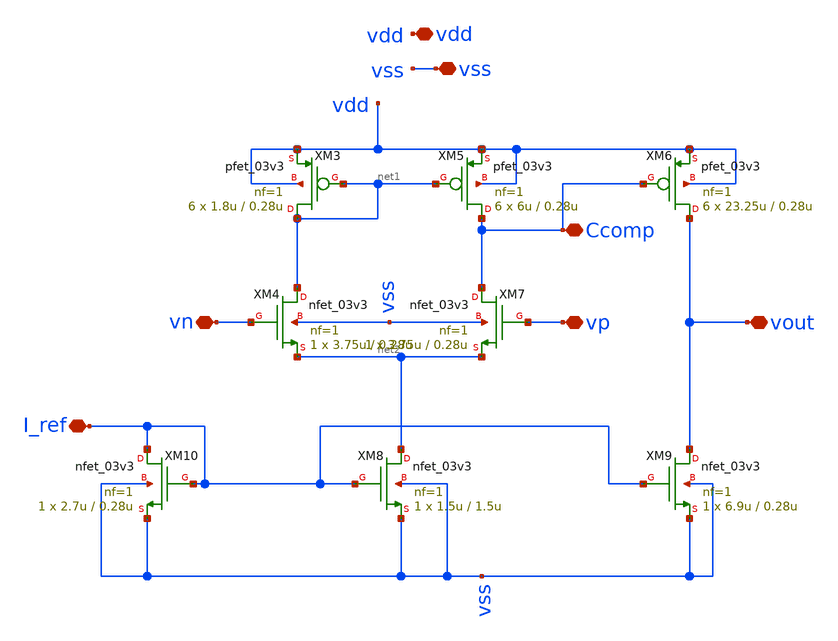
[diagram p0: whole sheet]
** sch_path: designs/libs/core_LIF_comp/core_ota_2stage/ota_2stage.sch
**.subckt ota_2stage vdd vss vn vp vout Ccomp I_ref
*.iopin vdd
*.iopin vss
*.iopin vn
*.iopin vp
*.iopin vout
*.iopin Ccomp
*.iopin I_ref
XM3 net1 net1 vdd vdd pfet_03v3 L=0.28u W=1.8u nf=1 ad='int((nf+1)/2) * W/nf * 0.18u' as='int((nf+2)/2) * W/nf * 0.18u'
+ pd='2*int((nf+1)/2) * (W/nf + 0.18u)' ps='2*int((nf+2)/2) * (W/nf + 0.18u)' nrd='0.18u / W' nrs='0.18u / W'
+ sa=0 sb=0 sd=0 m=6
XM4 net1 vn net2 vss nfet_03v3 L=0.28u W=3.75u nf=1 ad='int((nf+1)/2) * W/nf * 0.18u' as='int((nf+2)/2) * W/nf * 0.18u'
+ pd='2*int((nf+1)/2) * (W/nf + 0.18u)' ps='2*int((nf+2)/2) * (W/nf + 0.18u)' nrd='0.18u / W' nrs='0.18u / W'
+ sa=0 sb=0 sd=0 m=1
XM5 Ccomp net1 vdd vdd pfet_03v3 L=0.28u W=6u nf=1 ad='int((nf+1)/2) * W/nf * 0.18u' as='int((nf+2)/2) * W/nf * 0.18u'
+ pd='2*int((nf+1)/2) * (W/nf + 0.18u)' ps='2*int((nf+2)/2) * (W/nf + 0.18u)' nrd='0.18u / W' nrs='0.18u / W'
+ sa=0 sb=0 sd=0 m=6
XM6 vout Ccomp vdd vdd pfet_03v3 L=0.28u W=23.25u nf=1 ad='int((nf+1)/2) * W/nf * 0.18u' as='int((nf+2)/2) * W/nf * 0.18u'
+ pd='2*int((nf+1)/2) * (W/nf + 0.18u)' ps='2*int((nf+2)/2) * (W/nf + 0.18u)' nrd='0.18u / W' nrs='0.18u / W'
+ sa=0 sb=0 sd=0 m=6
XM7 Ccomp vp net2 vss nfet_03v3 L=0.28u W=3.75u nf=1 ad='int((nf+1)/2) * W/nf * 0.18u' as='int((nf+2)/2) * W/nf * 0.18u'
+ pd='2*int((nf+1)/2) * (W/nf + 0.18u)' ps='2*int((nf+2)/2) * (W/nf + 0.18u)' nrd='0.18u / W' nrs='0.18u / W'
+ sa=0 sb=0 sd=0 m=1
XM8 net2 I_ref vss vss nfet_03v3 L=1.5u W=1.5u nf=1 ad='int((nf+1)/2) * W/nf * 0.18u' as='int((nf+2)/2) * W/nf * 0.18u'
+ pd='2*int((nf+1)/2) * (W/nf + 0.18u)' ps='2*int((nf+2)/2) * (W/nf + 0.18u)' nrd='0.18u / W' nrs='0.18u / W'
+ sa=0 sb=0 sd=0 m=1
XM9 vout I_ref vss vss nfet_03v3 L=0.28u W=6.9u nf=1 ad='int((nf+1)/2) * W/nf * 0.18u' as='int((nf+2)/2) * W/nf * 0.18u'
+ pd='2*int((nf+1)/2) * (W/nf + 0.18u)' ps='2*int((nf+2)/2) * (W/nf + 0.18u)' nrd='0.18u / W' nrs='0.18u / W'
+ sa=0 sb=0 sd=0 m=1
XM10 I_ref I_ref vss vss nfet_03v3 L=0.28u W=2.7u nf=1 ad='int((nf+1)/2) * W/nf * 0.18u' as='int((nf+2)/2) * W/nf * 0.18u'
+ pd='2*int((nf+1)/2) * (W/nf + 0.18u)' ps='2*int((nf+2)/2) * (W/nf + 0.18u)' nrd='0.18u / W' nrs='0.18u / W'
+ sa=0 sb=0 sd=0 m=1
**.ends
.end
